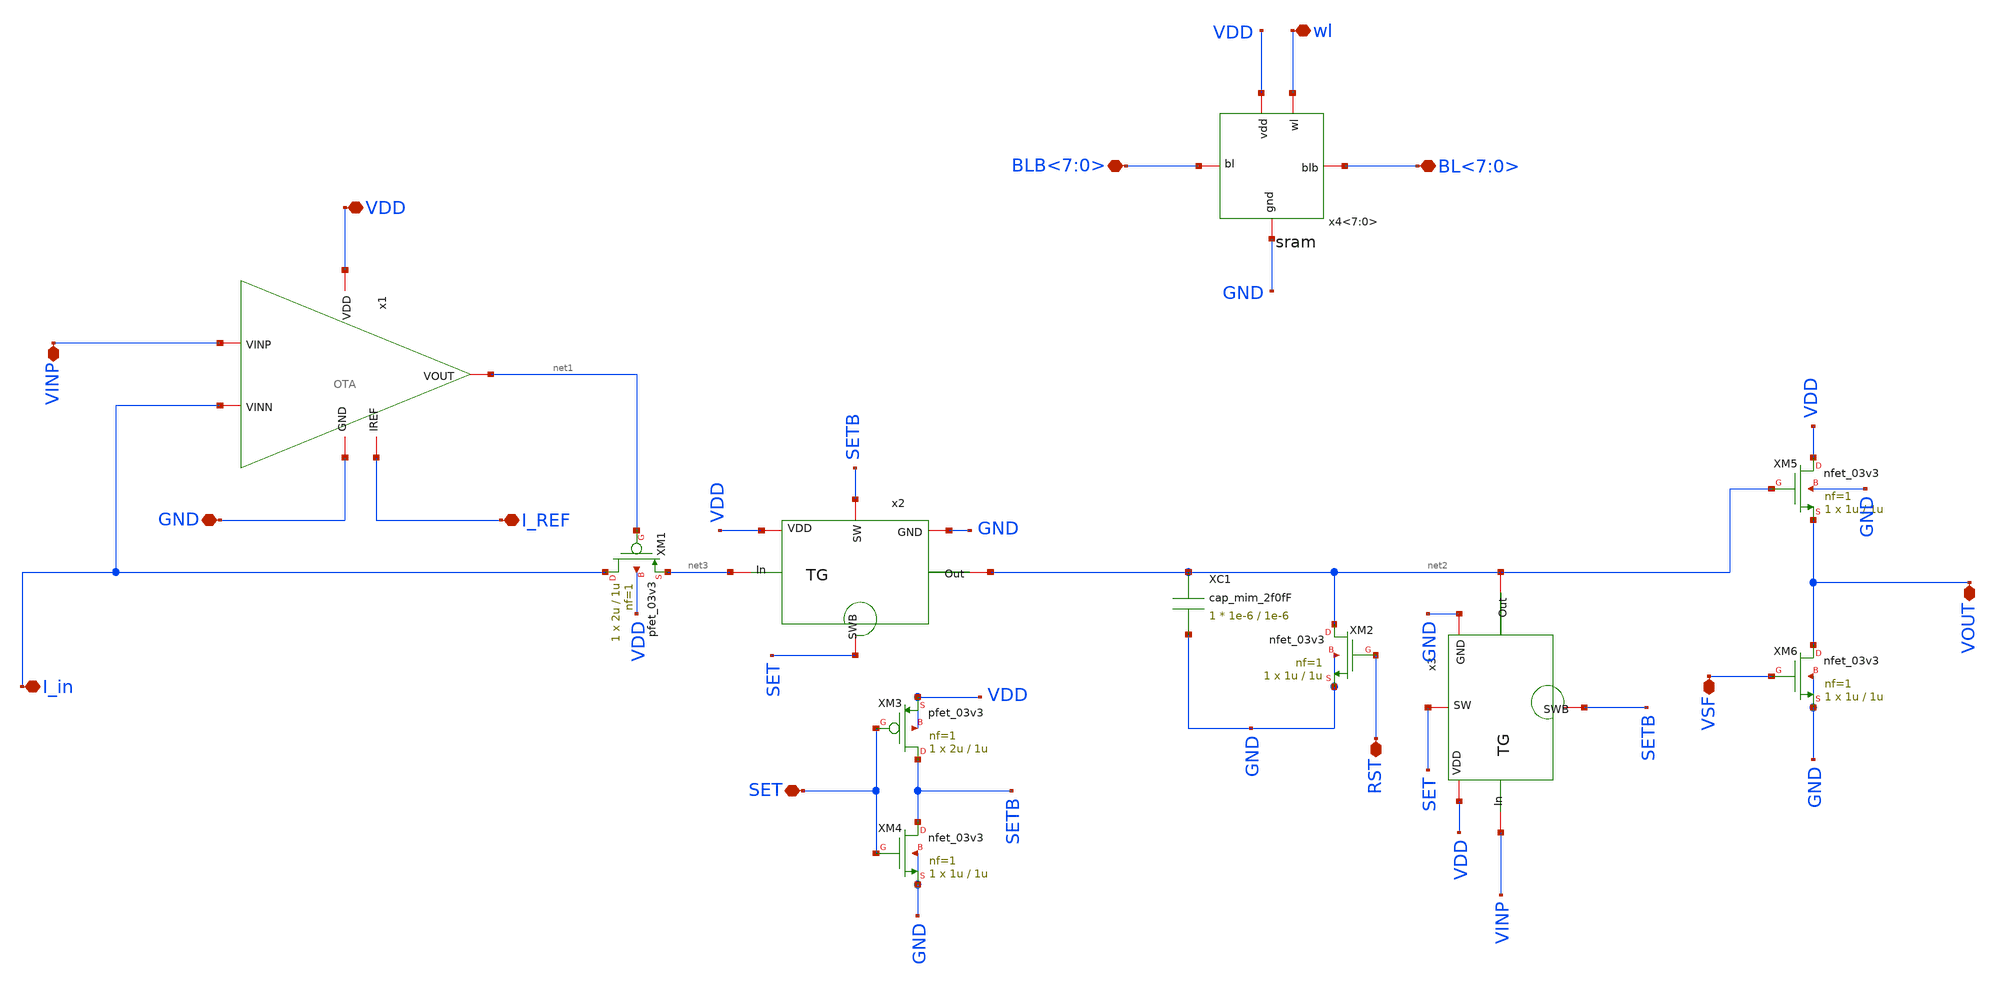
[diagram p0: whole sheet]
** sch_path: src/Pixel/FullPV0.sch
**.subckt FullPV0 VINP I_in I_REF GND VDD RST SET VSF VOUT wl BL<7:0> BLB<7:0>
*.iopin VINP
*.iopin I_in
*.iopin I_REF
*.iopin GND
*.iopin VDD
*.iopin RST
*.iopin SET
*.iopin VSF
*.iopin VOUT
*.iopin wl
*.iopin BL<7:0>
*.iopin BLB<7:0>
x1 VDD net1 VINP I_in I_REF GND OTA
XM1 I_in net1 net3 VDD pfet_03v3 L=1u W=2u nf=1 ad='int((nf+1)/2) * W/nf * 0.18u' as='int((nf+2)/2) * W/nf * 0.18u'
+ pd='2*int((nf+1)/2) * (W/nf + 0.18u)' ps='2*int((nf+2)/2) * (W/nf + 0.18u)' nrd='0.18u / W' nrs='0.18u / W'
+ sa=0 sb=0 sd=0 m=1
XC1 net2 GND cap_mim_2f0fF c_width=1e-6 c_length=1e-6 m=1
XM2 net2 RST GND GND nfet_03v3 L=1u W=1u nf=1 ad='int((nf+1)/2) * W/nf * 0.18u' as='int((nf+2)/2) * W/nf * 0.18u'
+ pd='2*int((nf+1)/2) * (W/nf + 0.18u)' ps='2*int((nf+2)/2) * (W/nf + 0.18u)' nrd='0.18u / W' nrs='0.18u / W'
+ sa=0 sb=0 sd=0 m=1
x2 net3 SETB SET VDD GND net2 TG
XM3 SETB SET VDD VDD pfet_03v3 L=1u W=2u nf=1 ad='int((nf+1)/2) * W/nf * 0.18u' as='int((nf+2)/2) * W/nf * 0.18u'
+ pd='2*int((nf+1)/2) * (W/nf + 0.18u)' ps='2*int((nf+2)/2) * (W/nf + 0.18u)' nrd='0.18u / W' nrs='0.18u / W'
+ sa=0 sb=0 sd=0 m=1
XM4 SETB SET GND GND nfet_03v3 L=1u W=1u nf=1 ad='int((nf+1)/2) * W/nf * 0.18u' as='int((nf+2)/2) * W/nf * 0.18u'
+ pd='2*int((nf+1)/2) * (W/nf + 0.18u)' ps='2*int((nf+2)/2) * (W/nf + 0.18u)' nrd='0.18u / W' nrs='0.18u / W'
+ sa=0 sb=0 sd=0 m=1
x3 VINP SET SETB VDD GND net2 TG
XM5 VDD net2 VOUT GND nfet_03v3 L=1u W=1u nf=1 ad='int((nf+1)/2) * W/nf * 0.18u' as='int((nf+2)/2) * W/nf * 0.18u'
+ pd='2*int((nf+1)/2) * (W/nf + 0.18u)' ps='2*int((nf+2)/2) * (W/nf + 0.18u)' nrd='0.18u / W' nrs='0.18u / W'
+ sa=0 sb=0 sd=0 m=1
XM6 VOUT VSF GND GND nfet_03v3 L=1u W=1u nf=1 ad='int((nf+1)/2) * W/nf * 0.18u' as='int((nf+2)/2) * W/nf * 0.18u'
+ pd='2*int((nf+1)/2) * (W/nf + 0.18u)' ps='2*int((nf+2)/2) * (W/nf + 0.18u)' nrd='0.18u / W' nrs='0.18u / W'
+ sa=0 sb=0 sd=0 m=1
x4<7:0> VDD wl BL<7:0> BLB<7:0> GND sram
**.ends
.end
